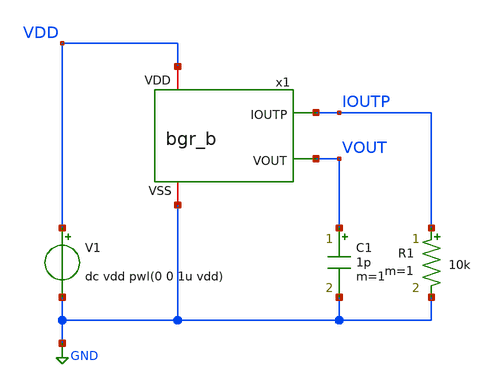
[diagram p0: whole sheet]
** sch_path: member_project/BGR/Maehashi/design/tb_bgr_b.sch
**.subckt tb_bgr_b
x1 VDD IOUTP VOUT GND bgr_b
V1 VDD GND dc vdd pwl(0 0 1u vdd)
C1 VOUT GND 1p m=1
R1 IOUTP GND 10k m=1
**** begin user architecture code


.option savecurrents
.temp 40
.param vdd = 5
.control
set units=degree
save all

alterparam vthMN = 0.1 ; Slow:0.1, Fast:-0.1
alterparam vthMP = 0.1 ; Slow:-0.1, Fast:0.1
alterparam magRS = 1 ; Slow:1.2, Fast:0.85
reset

tran 10ns 30us
gnuplot bgrbTranStartup_SF v(VDD) v(VOUT)
*plot v(VOUT) ylimit 0 1.2 xlabel Time ylabel Vbgr
*plot @m.x1.xmp3.m1[id] xlabel Temp ylabel Iout

.endc

 .include $::LIB/ip62_models
**** end user architecture code
**.ends
.GLOBAL GND
.end
